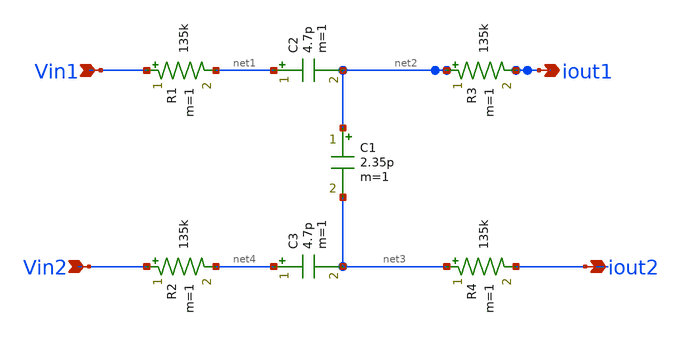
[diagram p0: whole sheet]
** sch_path: wienbridge1.sch
**.subckt wienbridge1 Vin1 Vin2 iout1 iout2
*.ipin Vin1
*.ipin Vin2
*.opin iout1
*.opin iout2
R1 Vin1 net1 135k m=1
R2 Vin2 net4 135k m=1
R3 net2 iout1 135k m=1
R4 net3 iout2 135k m=1
C1 net2 net3 2.35p m=1
C2 net1 net2 4.7p m=1
C3 net4 net3 4.7p m=1
**.ends
.end
